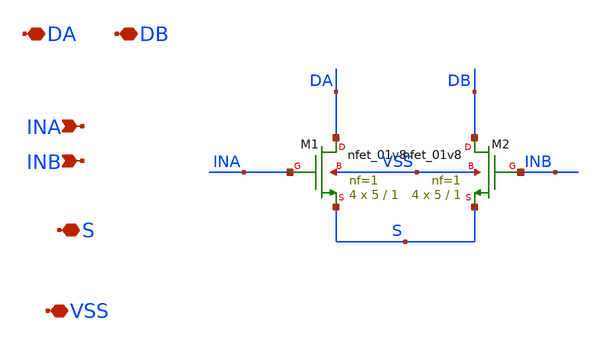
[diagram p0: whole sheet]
** sch_path: xschem/indiff.sch
**.subckt indiff INA INB DA DB S VSS
*.ipin INA
*.ipin INB
*.iopin DA
*.iopin DB
*.iopin S
*.iopin VSS
XM1 DA INA S VSS sky130_fd_pr__nfet_01v8 L=1 W=5 nf=1 ad='int((nf+1)/2) * W/nf * 0.29' as='int((nf+2)/2) * W/nf * 0.29'
+ pd='2*int((nf+1)/2) * (W/nf + 0.29)' ps='2*int((nf+2)/2) * (W/nf + 0.29)' nrd='0.29 / W' nrs='0.29 / W'
+ sa=0 sb=0 sd=0 mult=4 m=4
XM2 DB INB S VSS sky130_fd_pr__nfet_01v8 L=1 W=5 nf=1 ad='int((nf+1)/2) * W/nf * 0.29' as='int((nf+2)/2) * W/nf * 0.29'
+ pd='2*int((nf+1)/2) * (W/nf + 0.29)' ps='2*int((nf+2)/2) * (W/nf + 0.29)' nrd='0.29 / W' nrs='0.29 / W'
+ sa=0 sb=0 sd=0 mult=4 m=4
**.ends
.end
